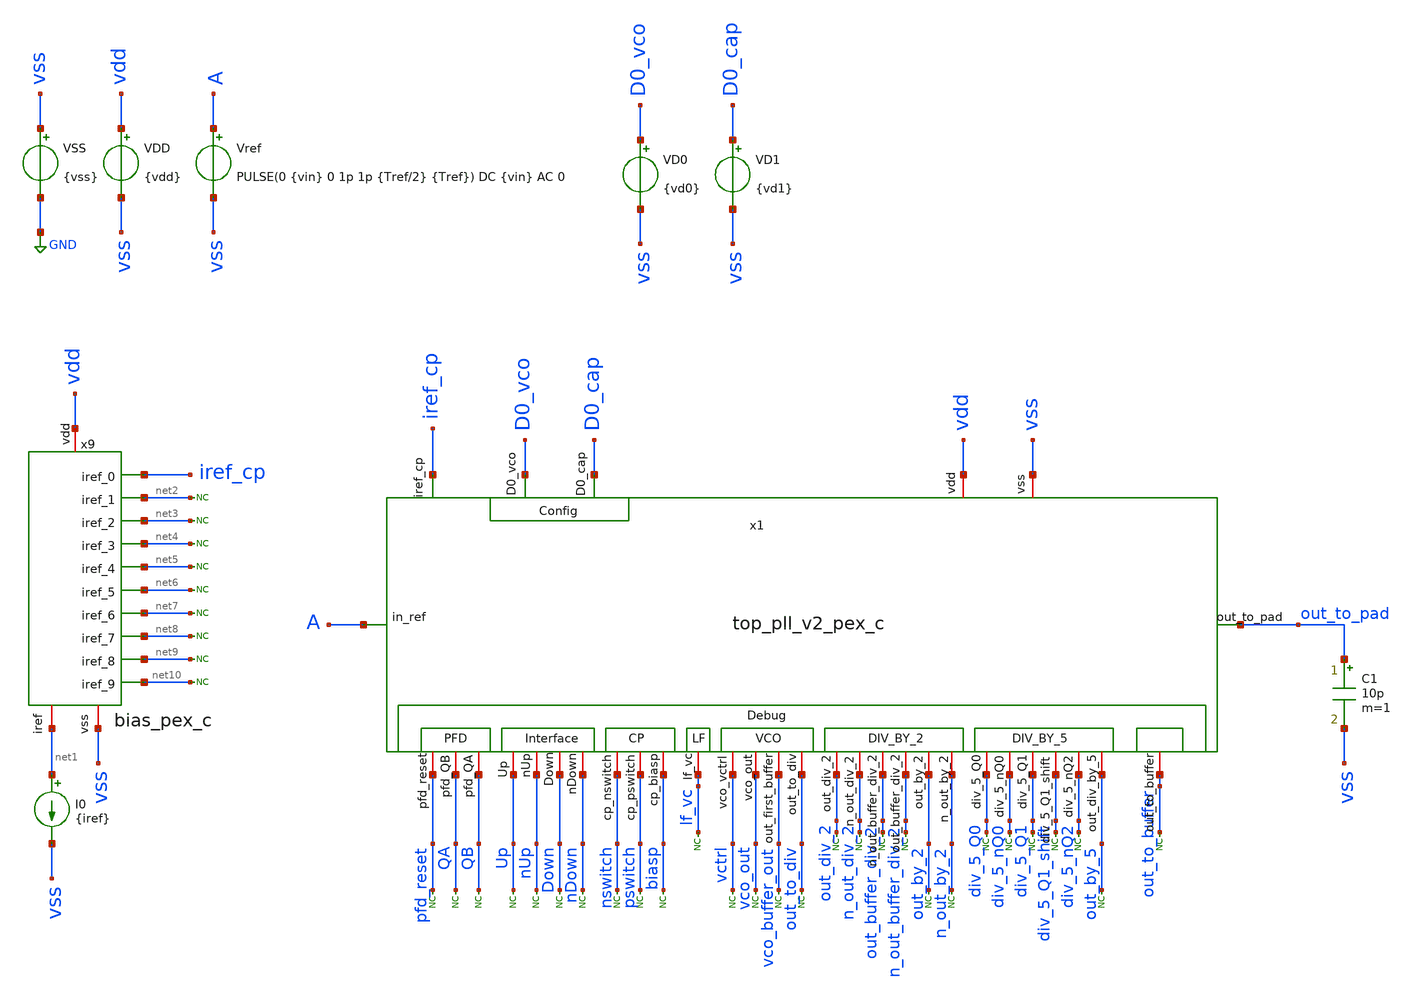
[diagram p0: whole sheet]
** sch_path: xschem/tb_top_pll_v2_pex_c.sch
**.subckt tb_top_pll_v2_pex_c
VSS vss GND {vss}
VDD vdd vss {vdd}
Vref A vss PULSE(0 {vin} 0 1p 1p {Tref/2} {Tref}) DC {vin} AC 0
VD0 D0_vco vss {vd0}
I0 net1 vss {iref}
* noconn #net2
* noconn #net3
* noconn #net4
* noconn #net5
* noconn #net6
* noconn #net7
* noconn #net8
* noconn #net9
* noconn #net10
* noconn div_5_nQ2
* noconn div_5_Q1_shift
* noconn div_5_Q1
* noconn div_5_nQ0
* noconn div_5_Q0
* noconn n_out_buffer_div_2
* noconn out_buffer_div_2
* noconn n_out_div_2
* noconn out_div_2
* noconn nswitch
* noconn pswitch
* noconn biasp
* noconn pfd_reset
* noconn QA
* noconn QB
* noconn Up
* noconn nUp
* noconn Down
* noconn nDown
* noconn lf_vc
* noconn vctrl
* noconn vco_out
* noconn vco_buffer_out
* noconn out_to_div
* noconn out_by_2
* noconn n_out_by_2
* noconn out_by_5
x9 vdd net1 vss iref_cp net2 net3 net4 net5 net6 net7 net8 net9 net10 bias_pex_c
C1 out_to_pad vss 10p m=1
* noconn out_to_buffer
x1 iref_cp vss vdd vco_out vctrl Up QB nUp A out_to_pad Down nDown QA D0_vco lf_vc vco_buffer_out
+ biasp pswitch pfd_reset nswitch out_by_2 out_to_div out_by_5 n_out_by_2 div_5_nQ0 div_5_Q1_shift div_5_Q1
+ out_buffer_div_2 n_out_buffer_div_2 div_5_Q0 n_out_div_2 div_5_nQ2 out_div_2 out_to_buffer D0_cap top_pll_v2_pex_c
VD1 D0_cap vss {vd1}
**** begin user architecture code



* Parameters
.param kp = 1.0
.param vdd = kp*1.8
.param vss = 0.0
.param vin = vdd
.param fref = 100e6
.param Tref = 1/fref
.param iref = 100u
.param vd0 = 0.0
.param vd1 = 0.0

.options TEMP = 100.0
.options RSHUNT = 1e20

* Models
.lib ~/skywater/skywater-pdk/libraries/sky130_fd_pr_ngspice/latest/models/corners/sky130.lib FF
.include ~/caravel_analog_fulgor/xschem/simulations/top_pll_v2_pex_c.spice
.include ~/caravel_analog_fulgor/xschem/simulations/bias_pex_c.spice

* Data to save

.ic v(A) = 0.0
.ic v(QA) = 0.0
.ic v(QB) = 0.0
.ic v(Up) = 0.0
.ic v(nUp) = 0.0
.ic v(Down) = 0.0
.ic v(nDown) = 0.0
.ic v(vctrl) = 0.0
.ic v(D0) = 0.0
.ic v(vco_out) = 0.0
.ic v(vco_buffer_out) = 0.0
.ic v(out_to_div) = 0.0
.ic v(out_to_pad) = 0.0
.ic v(out_div_2) = 0.0
.ic v(n_out_div_2) = 0.0
.ic v(out_buffer_div_2) = 0.0
.ic v(n_out_buffer_div_2) = 0.0
.ic v(out_by_2) = 0.0
.ic v(n_out_by_2) = 0.0
.ic v(div_5_Q0) = 0.0
.ic v(div_5_nQ0) = 0.0
.ic v(div_5_Q1) = 0.0
.ic v(div_5_Q1_shift) = 0.0
.ic v(div_5_nQ2) = 0.0
.ic v(out_by_5) = 0.0

* Simulation
.control
	tran 0.01ns 1.5us
	meas tran Tosc trig v(out_to_div) val=0.9 fall=1005 targ v(out_to_div) val=0.9 fall=1105
	let  T = Tosc/100.0
	let  f = 1/T
	echo .
	echo ------ PLL simulation ------
	print T f
	*write tb_PLL_tran.raw
	plot v(vctrl) v(pfd_reset)+2 v(nDown)+4 v(Down)+6 v(nUp)+8 v(Up)+10 v(QA)+12 v(QB)+12 v(A)+14
+ v(out_by_5)+16
 	plot v(out_to_pad)+12 v(out_to_buffer)+9 (out_to_div)+6 v(out_by_2)+3 v(out_by_5)
	plot v(out_by_5) v(out_by_2) v(out_to_div)
	plot v(vctrl)
	plot v(pswitch) v(nswitch) xlimit 1.4us 1.444us
.endc

.end


**** end user architecture code
**.ends
.GLOBAL GND
.end
